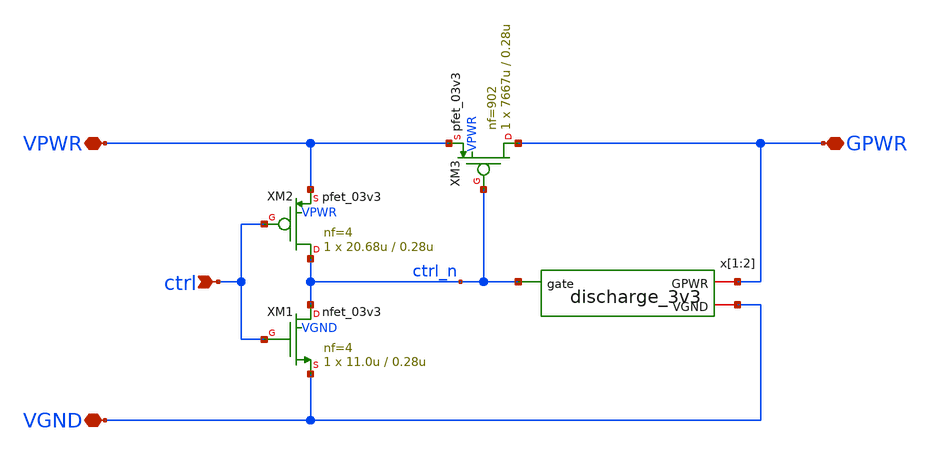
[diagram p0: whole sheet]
** sch_path: pg/gf180mcuD/tt_pg_3v3_hp_4/xschem/tt_pg_3v3_hp_4.sch
**.subckt tt_pg_3v3_hp_4 ctrl VPWR VGND GPWR
*.ipin ctrl
*.iopin VPWR
*.iopin VGND
*.iopin GPWR
x[1] VGND GPWR ctrl_n discharge_3v3
x[2] VGND GPWR ctrl_n discharge_3v3
XM1 ctrl_n ctrl VGND VGND nfet_03v3 L=0.28u W=11.0u nf=4 ad='int((nf+1)/2) * W/nf * 0.18u' as='int((nf+2)/2) * W/nf * 0.18u'
+ pd='2*int((nf+1)/2) * (W/nf + 0.18u)' ps='2*int((nf+2)/2) * (W/nf + 0.18u)' nrd='0.18u / W' nrs='0.18u / W'
+ sa=0 sb=0 sd=0 m=1 par=1
XM2 ctrl_n ctrl VPWR VPWR pfet_03v3 L=0.28u W=20.68u nf=4 ad='int((nf+1)/2) * W/nf * 0.18u' as='int((nf+2)/2) * W/nf * 0.18u'
+ pd='2*int((nf+1)/2) * (W/nf + 0.18u)' ps='2*int((nf+2)/2) * (W/nf + 0.18u)' nrd='0.18u / W' nrs='0.18u / W'
+ sa=0 sb=0 sd=0 m=1 par=1
XM3 GPWR ctrl_n VPWR VPWR pfet_03v3 L=0.28u W=7667u nf=902 ad='int((nf+1)/2) * W/nf * 0.18u' as='int((nf+2)/2) * W/nf * 0.18u'
+ pd='2*int((nf+1)/2) * (W/nf + 0.18u)' ps='2*int((nf+2)/2) * (W/nf + 0.18u)' nrd='0.18u / W' nrs='0.18u / W'
+ sa=0 sb=0 sd=0 m=1 par=1
**.ends

* expanding   symbol:  discharge_3v3.sym # of pins=3
** sym_path: pg/gf180mcuD/common/xschem/discharge_3v3.sym
** sch_path: pg/gf180mcuD/common/xschem/discharge_3v3.sch
.subckt discharge_3v3 VGND GPWR gate
*.iopin GPWR
*.iopin VGND
*.ipin gate
XM1 GPWR gate net3 VGND nfet_03v3 L=0.6u W=0.99u nf=1 ad='int((nf+1)/2) * W/nf * 0.18u' as='int((nf+2)/2) * W/nf * 0.18u'
+ pd='2*int((nf+1)/2) * (W/nf + 0.18u)' ps='2*int((nf+2)/2) * (W/nf + 0.18u)' nrd='0.18u / W' nrs='0.18u / W'
+ sa=0 sb=0 sd=0 m=1 par=1
XM2 net3 gate net2 VGND nfet_03v3 L=0.6u W=0.99u nf=1 ad='int((nf+1)/2) * W/nf * 0.18u' as='int((nf+2)/2) * W/nf * 0.18u'
+ pd='2*int((nf+1)/2) * (W/nf + 0.18u)' ps='2*int((nf+2)/2) * (W/nf + 0.18u)' nrd='0.18u / W' nrs='0.18u / W'
+ sa=0 sb=0 sd=0 m=1 par=1
XM3 net2 gate net1 VGND nfet_03v3 L=0.6u W=0.99u nf=1 ad='int((nf+1)/2) * W/nf * 0.18u' as='int((nf+2)/2) * W/nf * 0.18u'
+ pd='2*int((nf+1)/2) * (W/nf + 0.18u)' ps='2*int((nf+2)/2) * (W/nf + 0.18u)' nrd='0.18u / W' nrs='0.18u / W'
+ sa=0 sb=0 sd=0 m=1 par=1
XM4 net1 gate VGND VGND nfet_03v3 L=0.6u W=0.99u nf=1 ad='int((nf+1)/2) * W/nf * 0.18u' as='int((nf+2)/2) * W/nf * 0.18u'
+ pd='2*int((nf+1)/2) * (W/nf + 0.18u)' ps='2*int((nf+2)/2) * (W/nf + 0.18u)' nrd='0.18u / W' nrs='0.18u / W'
+ sa=0 sb=0 sd=0 m=1 par=1
XM5 GPWR gate net6 VGND nfet_03v3 L=0.6u W=0.99u nf=1 ad='int((nf+1)/2) * W/nf * 0.18u' as='int((nf+2)/2) * W/nf * 0.18u'
+ pd='2*int((nf+1)/2) * (W/nf + 0.18u)' ps='2*int((nf+2)/2) * (W/nf + 0.18u)' nrd='0.18u / W' nrs='0.18u / W'
+ sa=0 sb=0 sd=0 m=1 par=1
XM6 net6 gate net5 VGND nfet_03v3 L=0.6u W=0.99u nf=1 ad='int((nf+1)/2) * W/nf * 0.18u' as='int((nf+2)/2) * W/nf * 0.18u'
+ pd='2*int((nf+1)/2) * (W/nf + 0.18u)' ps='2*int((nf+2)/2) * (W/nf + 0.18u)' nrd='0.18u / W' nrs='0.18u / W'
+ sa=0 sb=0 sd=0 m=1 par=1
XM7 net5 gate net4 VGND nfet_03v3 L=0.6u W=0.99u nf=1 ad='int((nf+1)/2) * W/nf * 0.18u' as='int((nf+2)/2) * W/nf * 0.18u'
+ pd='2*int((nf+1)/2) * (W/nf + 0.18u)' ps='2*int((nf+2)/2) * (W/nf + 0.18u)' nrd='0.18u / W' nrs='0.18u / W'
+ sa=0 sb=0 sd=0 m=1 par=1
XM8 net4 gate VGND VGND nfet_03v3 L=0.6u W=0.99u nf=1 ad='int((nf+1)/2) * W/nf * 0.18u' as='int((nf+2)/2) * W/nf * 0.18u'
+ pd='2*int((nf+1)/2) * (W/nf + 0.18u)' ps='2*int((nf+2)/2) * (W/nf + 0.18u)' nrd='0.18u / W' nrs='0.18u / W'
+ sa=0 sb=0 sd=0 m=1 par=1
.ends

.end
